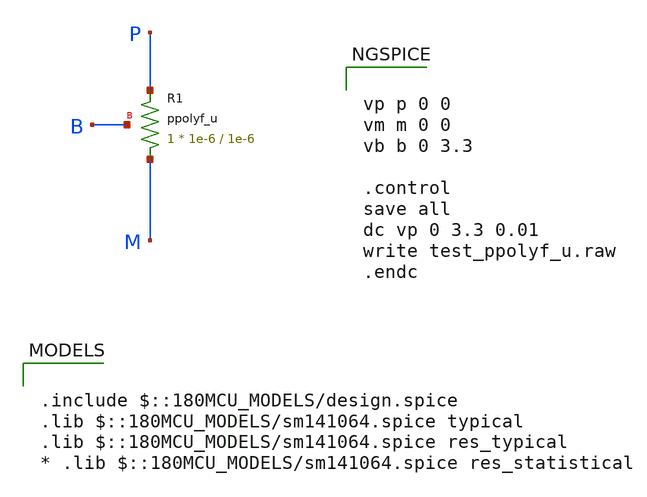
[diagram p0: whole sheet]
** sch_path: cells/xschem/tests/test_ppolyf_u.sch
* Copyright 2022 GlobalFoundries PDK Authors
* Licensed under the Apache License, Version 2.0 (the "License");
* you may not use this file except in compliance with the License.
* You may obtain a copy of the License at
* https://www.apache.org/licenses/LICENSE-2.0
* Unless required by applicable law or agreed to in writing, software
* distributed under the License is distributed on an "AS IS" BASIS,
* WITHOUT WARRANTIES OR CONDITIONS OF ANY KIND, either express or implied.
* See the License for the specific language governing permissions and
* limitations under the License.
**.subckt test_ppolyf_u
XR1 M P B ppolyf_u r_width=1e-6 r_length=1e-6 m=1
**** begin user architecture code

.include $::180MCU_MODELS/design.spice
.lib $::180MCU_MODELS/sm141064.spice typical
.lib $::180MCU_MODELS/sm141064.spice res_typical
* .lib $::180MCU_MODELS/sm141064.spice res_statistical



vp p 0 0
vm m 0 0
vb b 0 3.3

.control
save all
dc vp 0 3.3 0.01
write test_ppolyf_u.raw
.endc


**** end user architecture code
**.ends
.end
